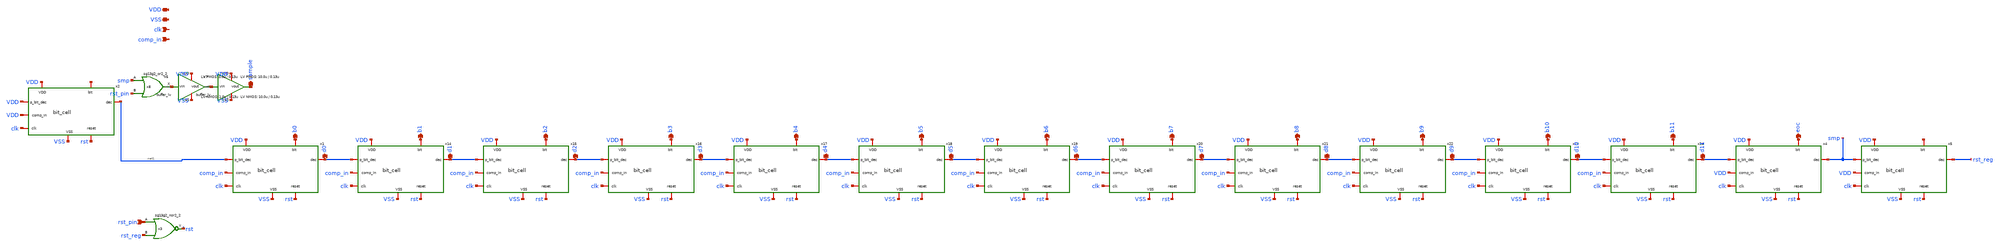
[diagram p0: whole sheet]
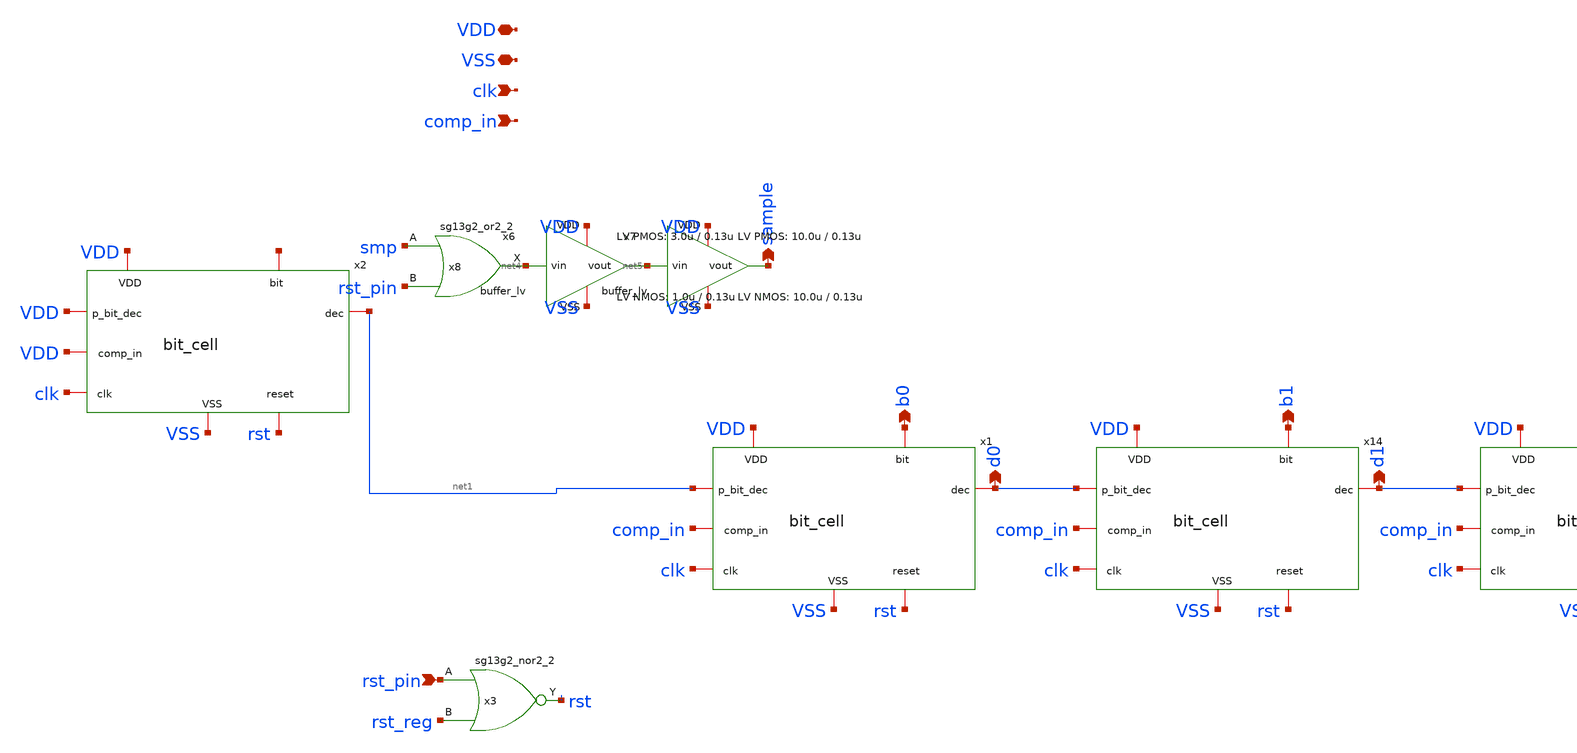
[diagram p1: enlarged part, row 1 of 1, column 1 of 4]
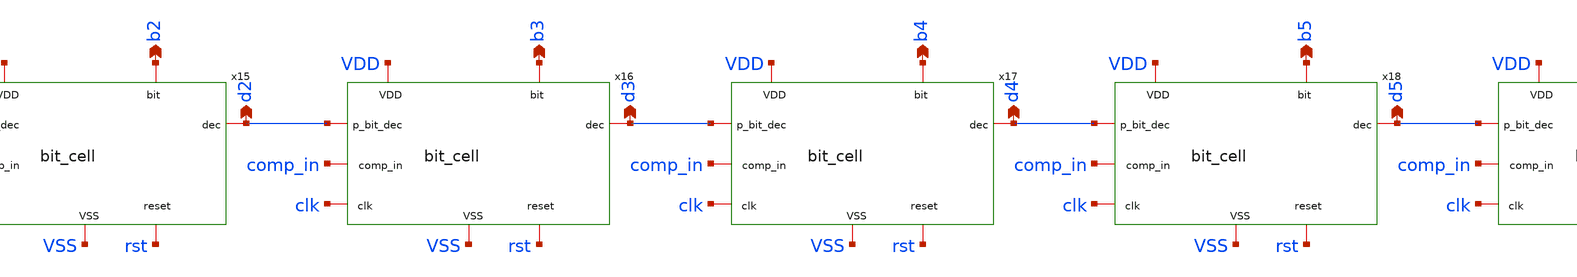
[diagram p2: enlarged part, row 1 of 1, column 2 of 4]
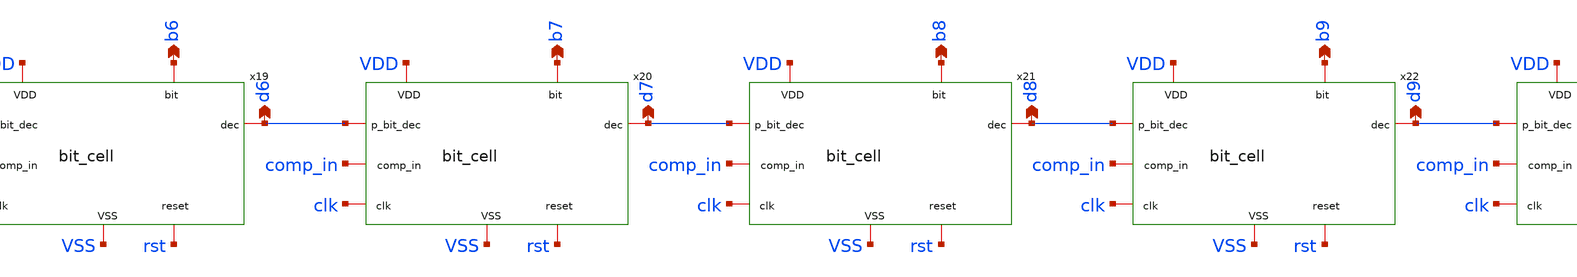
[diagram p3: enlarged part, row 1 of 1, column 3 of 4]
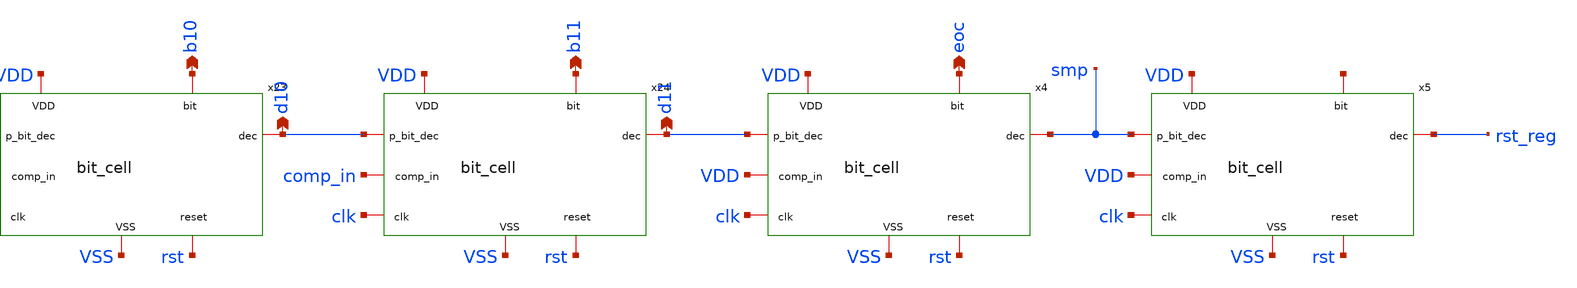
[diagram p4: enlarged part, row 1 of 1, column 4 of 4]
** sch_path: xschem/logic/logic.sch
**.subckt logic VDD VSS clk comp_in b0 d0 b1 d1 b2 d2 b3 d3 b4 d4 b5 d5 b6 d6 b7 d7 b8 d8 b9 d9 b10
*+ d10 b11 d11 rst_pin eoc sample
*.iopin VDD
*.iopin VSS
*.ipin clk
*.ipin comp_in
*.opin b0
*.opin d0
*.opin b1
*.opin d1
*.opin b2
*.opin d2
*.opin b3
*.opin d3
*.opin b4
*.opin d4
*.opin b5
*.opin d5
*.opin b6
*.opin d6
*.opin b7
*.opin d7
*.opin b8
*.opin d8
*.opin b9
*.opin d9
*.opin b10
*.opin d10
*.opin b11
*.opin d11
*.ipin rst_pin
*.opin eoc
*.opin sample
x1 clk net1 rst comp_in VDD b0 VSS d0 bit_cell
x14 clk d0 rst comp_in VDD b1 VSS d1 bit_cell
x15 clk d1 rst comp_in VDD b2 VSS d2 bit_cell
x16 clk d2 rst comp_in VDD b3 VSS d3 bit_cell
x17 clk d3 rst comp_in VDD b4 VSS d4 bit_cell
x18 clk d4 rst comp_in VDD b5 VSS d5 bit_cell
x19 clk d5 rst comp_in VDD b6 VSS d6 bit_cell
x20 clk d6 rst comp_in VDD b7 VSS d7 bit_cell
x21 clk d7 rst comp_in VDD b8 VSS d8 bit_cell
x22 clk d8 rst comp_in VDD b9 VSS d9 bit_cell
x23 clk d9 rst comp_in VDD b10 VSS d10 bit_cell
x24 clk d10 rst comp_in VDD b11 VSS d11 bit_cell
x3 rst rst_pin rst_reg VDD VSS sg13g2_nor2_2
x4 clk d11 rst VDD VDD eoc VSS smp bit_cell
x5 clk smp rst VDD VDD net2 VSS rst_reg bit_cell
x2 clk VDD rst VDD VDD net3 VSS net1 bit_cell
x6 VDD net4 net5 VSS buffer_lv W_P_INV=3.0u L_P_INV=0.13u W_N_INV=1.0u L_N_INV=0.13u
x7 VDD net5 sample VSS buffer_lv W_P_INV=10.0u L_P_INV=0.13u W_N_INV=10.0u L_N_INV=0.13u
x8 net4 smp rst_pin VDD VSS sg13g2_or2_2
**.ends
.end
